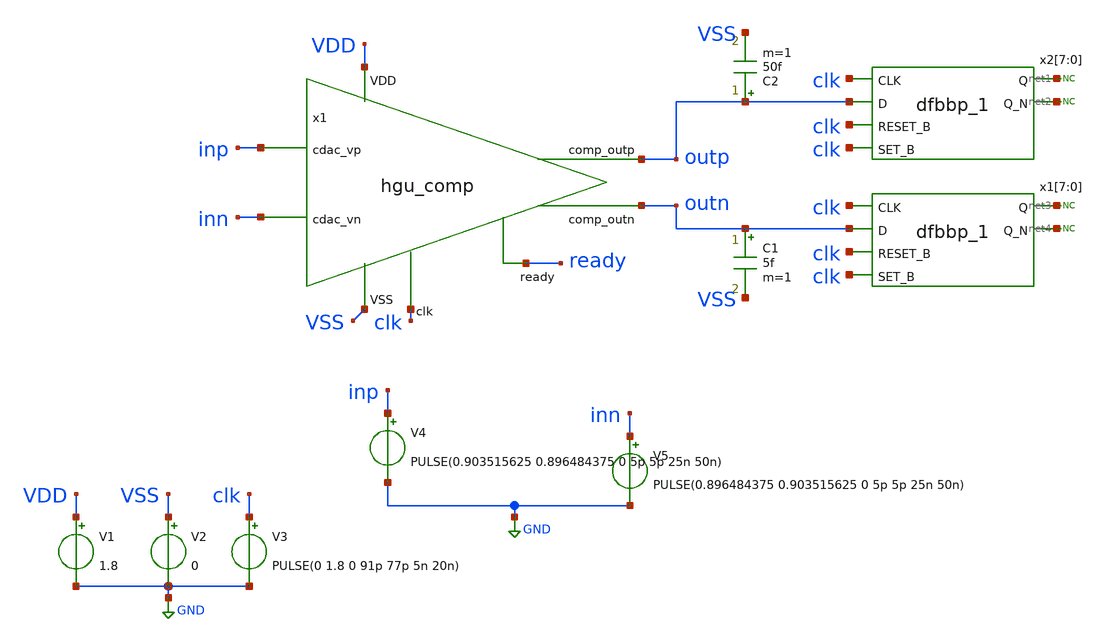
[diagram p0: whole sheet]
** sch_path: hgu/tb/tb_hgu_comp.sch
**.subckt tb_hgu_comp
x1 ready inn outp outn inp clk VDD VSS hgu_comp
V1 VDD GND 1.8
V2 VSS GND 0
V3 clk GND PULSE(0 1.8 0 91p 77p 5n 20n)
V4 inp GND PULSE(0.903515625 0.896484375 0 5p 5p 25n 50n)
V5 inn GND PULSE(0.896484375 0.903515625 0 5p 5p 25n 50n)
x2[7] clk outp clk clk VGND VNB VPB VPWR net1 net2 sky130_fd_sc_hd__dfbbp_1
x2[6] clk outp clk clk VGND VNB VPB VPWR net1 net2 sky130_fd_sc_hd__dfbbp_1
x2[5] clk outp clk clk VGND VNB VPB VPWR net1 net2 sky130_fd_sc_hd__dfbbp_1
x2[4] clk outp clk clk VGND VNB VPB VPWR net1 net2 sky130_fd_sc_hd__dfbbp_1
x2[3] clk outp clk clk VGND VNB VPB VPWR net1 net2 sky130_fd_sc_hd__dfbbp_1
x2[2] clk outp clk clk VGND VNB VPB VPWR net1 net2 sky130_fd_sc_hd__dfbbp_1
x2[1] clk outp clk clk VGND VNB VPB VPWR net1 net2 sky130_fd_sc_hd__dfbbp_1
x2[0] clk outp clk clk VGND VNB VPB VPWR net1 net2 sky130_fd_sc_hd__dfbbp_1
x1[7] clk outn clk clk VGND VNB VPB VPWR net3 net4 sky130_fd_sc_hd__dfbbp_1
x1[6] clk outn clk clk VGND VNB VPB VPWR net3 net4 sky130_fd_sc_hd__dfbbp_1
x1[5] clk outn clk clk VGND VNB VPB VPWR net3 net4 sky130_fd_sc_hd__dfbbp_1
x1[4] clk outn clk clk VGND VNB VPB VPWR net3 net4 sky130_fd_sc_hd__dfbbp_1
x1[3] clk outn clk clk VGND VNB VPB VPWR net3 net4 sky130_fd_sc_hd__dfbbp_1
x1[2] clk outn clk clk VGND VNB VPB VPWR net3 net4 sky130_fd_sc_hd__dfbbp_1
x1[1] clk outn clk clk VGND VNB VPB VPWR net3 net4 sky130_fd_sc_hd__dfbbp_1
x1[0] clk outn clk clk VGND VNB VPB VPWR net3 net4 sky130_fd_sc_hd__dfbbp_1
C1 outn VSS 5f m=1
C2 outp VSS 50f m=1
* noconn #net1
* noconn #net2
* noconn #net3
* noconn #net4
**** begin user architecture code


.include /foss/designs/hgu_goss/hgu/spice/hgu_comp_flat_RC.spice
.lib /foss/pdks/sky130A/libs.tech/ngspice/sky130.lib.spice tt
.include /foss/pdks/sky130A/libs.ref/sky130_fd_sc_hd/spice/sky130_fd_sc_hd.spice
.tran 0.1ns 100ns
.temp 25
.control
    run
     let svdd = 1.8
     let max = svdd*0.8
     let min = svdd*0.2
     let mid = svdd*0.5

   meas tran rising_s_d find time when V(clk)=mid RISE=1 TD=30n
   meas tran rising_e_d find time when V(outp)=mid RISE=1 TD=1000p
   let rising_delay = rising_e_d-rising_s_d

   meas tran falling_s_d find time when V(clk)=mid RISE=1 TD=50n
   meas tran falling_e_d find time when V(outp)=mid FALL=1 TD=50n
   let falling_delay = falling_e_d-falling_s_d

   meas tran rising_s find time when V(outp)=min RISE=1 TD=30n
      meas tran rising_e find time when V(outp)=max RISE=1 TD=30n
      let rising_time = rising_e-rising_s

      meas tran falling_s find time when V(outp)=max FALL=1 TD=50n
     meas tran falling_e find time when V(outp)=min FALL=1 TD=50n
      let falling_time = falling_e-falling_s

	meas tran I_avg AVG tran1.I(VDD) FROM=20n TO=100n

    print rising_time falling_time rising_delay falling_delay
    plot V(clk) V(inn) V(inp) V(ready) V(outp)+2 V(outn)+2

	*setplot tran1
	*linearize V(outp)
	*set specwindow=blackman
	*fft V(outp)
	*plot mag(V(outp))
.endc
.save all


**** end user architecture code
**.ends

* expanding   symbol:  ../xschem/hgu_comp.sym # of pins=8
** sym_path: hgu/xschem/hgu_comp.sym
** sch_path: hgu/xschem/hgu_comp.sch
.subckt hgu_comp ready cdac_vn comp_outp comp_outn cdac_vp clk VDD VSS
*.ipin cdac_vn
*.ipin cdac_vp
*.ipin VSS
*.ipin VDD
*.ipin clk
*.opin ready
*.opin comp_outp
*.opin comp_outn
XM1 net1 clk VSS VSS sky130_fd_pr__nfet_01v8 L=0.15 W=4 nf=4 ad='int((nf+1)/2) * W/nf * 0.29' as='int((nf+2)/2) * W/nf * 0.29'
+ pd='2*int((nf+1)/2) * (W/nf + 0.29)' ps='2*int((nf+2)/2) * (W/nf + 0.29)' nrd='0.29 / W' nrs='0.29 / W'
+ sa=0 sb=0 sd=0 mult=1 m=1
XM4 Y X Q VSS sky130_fd_pr__nfet_01v8 L=0.15 W=1 nf=1 ad='int((nf+1)/2) * W/nf * 0.29' as='int((nf+2)/2) * W/nf * 0.29'
+ pd='2*int((nf+1)/2) * (W/nf + 0.29)' ps='2*int((nf+2)/2) * (W/nf + 0.29)' nrd='0.29 / W' nrs='0.29 / W'
+ sa=0 sb=0 sd=0 mult=1 m=1
XM5 X Y P VSS sky130_fd_pr__nfet_01v8 L=0.15 W=1 nf=1 ad='int((nf+1)/2) * W/nf * 0.29' as='int((nf+2)/2) * W/nf * 0.29'
+ pd='2*int((nf+1)/2) * (W/nf + 0.29)' ps='2*int((nf+2)/2) * (W/nf + 0.29)' nrd='0.29 / W' nrs='0.29 / W'
+ sa=0 sb=0 sd=0 mult=1 m=1
XM6 X Y VDD VDD sky130_fd_pr__pfet_01v8 L=0.15 W=1 nf=1 ad='int((nf+1)/2) * W/nf * 0.29' as='int((nf+2)/2) * W/nf * 0.29'
+ pd='2*int((nf+1)/2) * (W/nf + 0.29)' ps='2*int((nf+2)/2) * (W/nf + 0.29)' nrd='0.29 / W' nrs='0.29 / W'
+ sa=0 sb=0 sd=0 mult=1 m=1
XM7 Y X VDD VDD sky130_fd_pr__pfet_01v8 L=0.15 W=1 nf=1 ad='int((nf+1)/2) * W/nf * 0.29' as='int((nf+2)/2) * W/nf * 0.29'
+ pd='2*int((nf+1)/2) * (W/nf + 0.29)' ps='2*int((nf+2)/2) * (W/nf + 0.29)' nrd='0.29 / W' nrs='0.29 / W'
+ sa=0 sb=0 sd=0 mult=1 m=1
XM8 X clk VDD VDD sky130_fd_pr__pfet_01v8 L=0.15 W=1 nf=1 ad='int((nf+1)/2) * W/nf * 0.29' as='int((nf+2)/2) * W/nf * 0.29'
+ pd='2*int((nf+1)/2) * (W/nf + 0.29)' ps='2*int((nf+2)/2) * (W/nf + 0.29)' nrd='0.29 / W' nrs='0.29 / W'
+ sa=0 sb=0 sd=0 mult=1 m=1
XM9 P clk VDD VDD sky130_fd_pr__pfet_01v8 L=0.15 W=1 nf=1 ad='int((nf+1)/2) * W/nf * 0.29' as='int((nf+2)/2) * W/nf * 0.29'
+ pd='2*int((nf+1)/2) * (W/nf + 0.29)' ps='2*int((nf+2)/2) * (W/nf + 0.29)' nrd='0.29 / W' nrs='0.29 / W'
+ sa=0 sb=0 sd=0 mult=1 m=1
XM10 Y clk VDD VDD sky130_fd_pr__pfet_01v8 L=0.15 W=1 nf=1 ad='int((nf+1)/2) * W/nf * 0.29' as='int((nf+2)/2) * W/nf * 0.29'
+ pd='2*int((nf+1)/2) * (W/nf + 0.29)' ps='2*int((nf+2)/2) * (W/nf + 0.29)' nrd='0.29 / W' nrs='0.29 / W'
+ sa=0 sb=0 sd=0 mult=1 m=1
XM11 Q clk VDD VDD sky130_fd_pr__pfet_01v8 L=0.15 W=1 nf=1 ad='int((nf+1)/2) * W/nf * 0.29' as='int((nf+2)/2) * W/nf * 0.29'
+ pd='2*int((nf+1)/2) * (W/nf + 0.29)' ps='2*int((nf+2)/2) * (W/nf + 0.29)' nrd='0.29 / W' nrs='0.29 / W'
+ sa=0 sb=0 sd=0 mult=1 m=1
XM16 RS_n RS_p VDD VDD sky130_fd_pr__pfet_01v8 L=0.15 W=0.84 nf=1 ad='int((nf+1)/2) * W/nf * 0.29' as='int((nf+2)/2) * W/nf * 0.29'
+ pd='2*int((nf+1)/2) * (W/nf + 0.29)' ps='2*int((nf+2)/2) * (W/nf + 0.29)' nrd='0.29 / W' nrs='0.29 / W'
+ sa=0 sb=0 sd=0 mult=1 m=1
XM17 RS_p RS_n VDD VDD sky130_fd_pr__pfet_01v8 L=0.15 W=0.84 nf=1 ad='int((nf+1)/2) * W/nf * 0.29' as='int((nf+2)/2) * W/nf * 0.29'
+ pd='2*int((nf+1)/2) * (W/nf + 0.29)' ps='2*int((nf+2)/2) * (W/nf + 0.29)' nrd='0.29 / W' nrs='0.29 / W'
+ sa=0 sb=0 sd=0 mult=1 m=1
XM19 RS_p Y_inv VSS VSS sky130_fd_pr__nfet_01v8 L=0.15 W=0.84 nf=1 ad='int((nf+1)/2) * W/nf * 0.29' as='int((nf+2)/2) * W/nf * 0.29'
+ pd='2*int((nf+1)/2) * (W/nf + 0.29)' ps='2*int((nf+2)/2) * (W/nf + 0.29)' nrd='0.29 / W' nrs='0.29 / W'
+ sa=0 sb=0 sd=0 mult=1 m=1
XM23 RS_n X_inv VSS VSS sky130_fd_pr__nfet_01v8 L=0.15 W=0.84 nf=1 ad='int((nf+1)/2) * W/nf * 0.29' as='int((nf+2)/2) * W/nf * 0.29'
+ pd='2*int((nf+1)/2) * (W/nf + 0.29)' ps='2*int((nf+2)/2) * (W/nf + 0.29)' nrd='0.29 / W' nrs='0.29 / W'
+ sa=0 sb=0 sd=0 mult=1 m=1
XM2 P cdac_vp net1 VSS sky130_fd_pr__nfet_01v8_lvt L=0.15 W=8 nf=8 ad='int((nf+1)/2) * W / nf * 0.29'
+ as='int((nf+2)/2) * W / nf * 0.29' pd='2*int((nf+1)/2) * (W / nf + 0.29)' ps='2*int((nf+2)/2) * (W / nf + 0.29)'
+ nrd='0.29 / W ' nrs='0.29 / W ' sa=0 sb=0 sd=0 mult=1 m=1
XM3 Q cdac_vn net1 VSS sky130_fd_pr__nfet_01v8_lvt L=0.15 W=8 nf=8 ad='int((nf+1)/2) * W / nf * 0.29'
+ as='int((nf+2)/2) * W / nf * 0.29' pd='2*int((nf+1)/2) * (W / nf + 0.29)' ps='2*int((nf+2)/2) * (W / nf + 0.29)'
+ nrd='0.29 / W ' nrs='0.29 / W ' sa=0 sb=0 sd=0 mult=1 m=1
XM12 X_inv X VDD VDD sky130_fd_pr__pfet_01v8 L=0.15 W=0.84 nf=1 ad='int((nf+1)/2) * W/nf * 0.29' as='int((nf+2)/2) * W/nf * 0.29'
+ pd='2*int((nf+1)/2) * (W/nf + 0.29)' ps='2*int((nf+2)/2) * (W/nf + 0.29)' nrd='0.29 / W' nrs='0.29 / W'
+ sa=0 sb=0 sd=0 mult=1 m=1
XM13 X_inv X VSS VSS sky130_fd_pr__nfet_01v8 L=0.15 W=0.42 nf=1 ad='int((nf+1)/2) * W/nf * 0.29' as='int((nf+2)/2) * W/nf * 0.29'
+ pd='2*int((nf+1)/2) * (W/nf + 0.29)' ps='2*int((nf+2)/2) * (W/nf + 0.29)' nrd='0.29 / W' nrs='0.29 / W'
+ sa=0 sb=0 sd=0 mult=1 m=1
XM14 X_drive X_inv VDD VDD sky130_fd_pr__pfet_01v8 L=0.15 W=2.52 nf=3 ad='int((nf+1)/2) * W/nf * 0.29'
+ as='int((nf+2)/2) * W/nf * 0.29' pd='2*int((nf+1)/2) * (W/nf + 0.29)' ps='2*int((nf+2)/2) * (W/nf + 0.29)'
+ nrd='0.29 / W' nrs='0.29 / W' sa=0 sb=0 sd=0 mult=1 m=1
XM15 X_drive X_inv VSS VSS sky130_fd_pr__nfet_01v8 L=0.15 W=1.38 nf=3 ad='int((nf+1)/2) * W/nf * 0.29'
+ as='int((nf+2)/2) * W/nf * 0.29' pd='2*int((nf+1)/2) * (W/nf + 0.29)' ps='2*int((nf+2)/2) * (W/nf + 0.29)'
+ nrd='0.29 / W' nrs='0.29 / W' sa=0 sb=0 sd=0 mult=1 m=1
XM18 Y_inv Y VDD VDD sky130_fd_pr__pfet_01v8 L=0.15 W=0.84 nf=1 ad='int((nf+1)/2) * W/nf * 0.29' as='int((nf+2)/2) * W/nf * 0.29'
+ pd='2*int((nf+1)/2) * (W/nf + 0.29)' ps='2*int((nf+2)/2) * (W/nf + 0.29)' nrd='0.29 / W' nrs='0.29 / W'
+ sa=0 sb=0 sd=0 mult=1 m=1
XM20 Y_inv Y VSS VSS sky130_fd_pr__nfet_01v8 L=0.15 W=0.42 nf=1 ad='int((nf+1)/2) * W/nf * 0.29' as='int((nf+2)/2) * W/nf * 0.29'
+ pd='2*int((nf+1)/2) * (W/nf + 0.29)' ps='2*int((nf+2)/2) * (W/nf + 0.29)' nrd='0.29 / W' nrs='0.29 / W'
+ sa=0 sb=0 sd=0 mult=1 m=1
XM21 Y_drive Y_inv VDD VDD sky130_fd_pr__pfet_01v8 L=0.15 W=2.52 nf=3 ad='int((nf+1)/2) * W/nf * 0.29'
+ as='int((nf+2)/2) * W/nf * 0.29' pd='2*int((nf+1)/2) * (W/nf + 0.29)' ps='2*int((nf+2)/2) * (W/nf + 0.29)'
+ nrd='0.29 / W' nrs='0.29 / W' sa=0 sb=0 sd=0 mult=1 m=1
XM22 Y_drive Y_inv VSS VSS sky130_fd_pr__nfet_01v8 L=0.15 W=1.38 nf=3 ad='int((nf+1)/2) * W/nf * 0.29'
+ as='int((nf+2)/2) * W/nf * 0.29' pd='2*int((nf+1)/2) * (W/nf + 0.29)' ps='2*int((nf+2)/2) * (W/nf + 0.29)'
+ nrd='0.29 / W' nrs='0.29 / W' sa=0 sb=0 sd=0 mult=1 m=1
XM24 net2 Y_drive X_drive VDD sky130_fd_pr__pfet_01v8 L=0.15 W=0.84 nf=1 ad='int((nf+1)/2) * W/nf * 0.29'
+ as='int((nf+2)/2) * W/nf * 0.29' pd='2*int((nf+1)/2) * (W/nf + 0.29)' ps='2*int((nf+2)/2) * (W/nf + 0.29)'
+ nrd='0.29 / W' nrs='0.29 / W' sa=0 sb=0 sd=0 mult=1 m=1
XM25 net2 X_drive Y_drive VDD sky130_fd_pr__pfet_01v8 L=0.15 W=0.84 nf=1 ad='int((nf+1)/2) * W/nf * 0.29'
+ as='int((nf+2)/2) * W/nf * 0.29' pd='2*int((nf+1)/2) * (W/nf + 0.29)' ps='2*int((nf+2)/2) * (W/nf + 0.29)'
+ nrd='0.29 / W' nrs='0.29 / W' sa=0 sb=0 sd=0 mult=1 m=1
XM26 net2 Y_drive net3 VSS sky130_fd_pr__nfet_01v8 L=0.15 W=0.84 nf=1 ad='int((nf+1)/2) * W/nf * 0.29'
+ as='int((nf+2)/2) * W/nf * 0.29' pd='2*int((nf+1)/2) * (W/nf + 0.29)' ps='2*int((nf+2)/2) * (W/nf + 0.29)'
+ nrd='0.29 / W' nrs='0.29 / W' sa=0 sb=0 sd=0 mult=1 m=1
XM27 net3 X_drive VSS VSS sky130_fd_pr__nfet_01v8 L=0.15 W=0.84 nf=1 ad='int((nf+1)/2) * W/nf * 0.29'
+ as='int((nf+2)/2) * W/nf * 0.29' pd='2*int((nf+1)/2) * (W/nf + 0.29)' ps='2*int((nf+2)/2) * (W/nf + 0.29)'
+ nrd='0.29 / W' nrs='0.29 / W' sa=0 sb=0 sd=0 mult=1 m=1
XM28 ready net2 VDD VDD sky130_fd_pr__pfet_01v8 L=0.15 W=0.84 nf=1 ad='int((nf+1)/2) * W/nf * 0.29' as='int((nf+2)/2) * W/nf * 0.29'
+ pd='2*int((nf+1)/2) * (W/nf + 0.29)' ps='2*int((nf+2)/2) * (W/nf + 0.29)' nrd='0.29 / W' nrs='0.29 / W'
+ sa=0 sb=0 sd=0 mult=1 m=1
XM29 ready net2 VSS VSS sky130_fd_pr__nfet_01v8 L=0.15 W=0.42 nf=1 ad='int((nf+1)/2) * W/nf * 0.29' as='int((nf+2)/2) * W/nf * 0.29'
+ pd='2*int((nf+1)/2) * (W/nf + 0.29)' ps='2*int((nf+2)/2) * (W/nf + 0.29)' nrd='0.29 / W' nrs='0.29 / W'
+ sa=0 sb=0 sd=0 mult=1 m=1
XM30 net4 RS_p VDD VDD sky130_fd_pr__pfet_01v8 L=0.15 W=0.84 nf=1 ad='int((nf+1)/2) * W/nf * 0.29' as='int((nf+2)/2) * W/nf * 0.29'
+ pd='2*int((nf+1)/2) * (W/nf + 0.29)' ps='2*int((nf+2)/2) * (W/nf + 0.29)' nrd='0.29 / W' nrs='0.29 / W'
+ sa=0 sb=0 sd=0 mult=1 m=1
XM31 net4 RS_p VSS VSS sky130_fd_pr__nfet_01v8 L=0.15 W=0.42 nf=1 ad='int((nf+1)/2) * W/nf * 0.29' as='int((nf+2)/2) * W/nf * 0.29'
+ pd='2*int((nf+1)/2) * (W/nf + 0.29)' ps='2*int((nf+2)/2) * (W/nf + 0.29)' nrd='0.29 / W' nrs='0.29 / W'
+ sa=0 sb=0 sd=0 mult=1 m=1
XM32 comp_outp net4 VDD VDD sky130_fd_pr__pfet_01v8 L=0.15 W=2.52 nf=3 ad='int((nf+1)/2) * W/nf * 0.29'
+ as='int((nf+2)/2) * W/nf * 0.29' pd='2*int((nf+1)/2) * (W/nf + 0.29)' ps='2*int((nf+2)/2) * (W/nf + 0.29)'
+ nrd='0.29 / W' nrs='0.29 / W' sa=0 sb=0 sd=0 mult=1 m=1
XM33 comp_outp net4 VSS VSS sky130_fd_pr__nfet_01v8 L=0.15 W=1.38 nf=3 ad='int((nf+1)/2) * W/nf * 0.29'
+ as='int((nf+2)/2) * W/nf * 0.29' pd='2*int((nf+1)/2) * (W/nf + 0.29)' ps='2*int((nf+2)/2) * (W/nf + 0.29)'
+ nrd='0.29 / W' nrs='0.29 / W' sa=0 sb=0 sd=0 mult=1 m=1
XM34 net5 RS_n VDD VDD sky130_fd_pr__pfet_01v8 L=0.15 W=0.84 nf=1 ad='int((nf+1)/2) * W/nf * 0.29' as='int((nf+2)/2) * W/nf * 0.29'
+ pd='2*int((nf+1)/2) * (W/nf + 0.29)' ps='2*int((nf+2)/2) * (W/nf + 0.29)' nrd='0.29 / W' nrs='0.29 / W'
+ sa=0 sb=0 sd=0 mult=1 m=1
XM35 net5 RS_n VSS VSS sky130_fd_pr__nfet_01v8 L=0.15 W=0.42 nf=1 ad='int((nf+1)/2) * W/nf * 0.29' as='int((nf+2)/2) * W/nf * 0.29'
+ pd='2*int((nf+1)/2) * (W/nf + 0.29)' ps='2*int((nf+2)/2) * (W/nf + 0.29)' nrd='0.29 / W' nrs='0.29 / W'
+ sa=0 sb=0 sd=0 mult=1 m=1
XM36 comp_outn net5 VDD VDD sky130_fd_pr__pfet_01v8 L=0.15 W=2.52 nf=3 ad='int((nf+1)/2) * W/nf * 0.29'
+ as='int((nf+2)/2) * W/nf * 0.29' pd='2*int((nf+1)/2) * (W/nf + 0.29)' ps='2*int((nf+2)/2) * (W/nf + 0.29)'
+ nrd='0.29 / W' nrs='0.29 / W' sa=0 sb=0 sd=0 mult=1 m=1
XM37 comp_outn net5 VSS VSS sky130_fd_pr__nfet_01v8 L=0.15 W=1.38 nf=3 ad='int((nf+1)/2) * W/nf * 0.29'
+ as='int((nf+2)/2) * W/nf * 0.29' pd='2*int((nf+1)/2) * (W/nf + 0.29)' ps='2*int((nf+2)/2) * (W/nf + 0.29)'
+ nrd='0.29 / W' nrs='0.29 / W' sa=0 sb=0 sd=0 mult=1 m=1
.ends

.GLOBAL GND
.end
